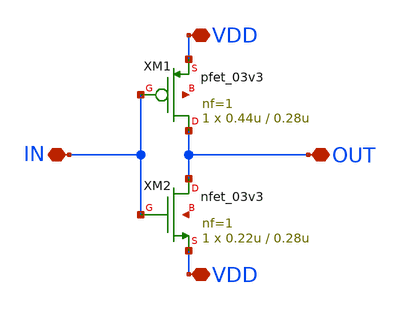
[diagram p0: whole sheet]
** sch_path: inverter.sch
**.subckt inverter OUT IN VDD VDD
*.iopin OUT
*.iopin IN
*.iopin VDD
*.iopin VDD
XM1 OUT IN VDD net1 pfet_03v3 L=0.28u W=0.44u nf=1 ad='int((nf+1)/2) * W/nf * 0.18u' as='int((nf+2)/2) * W/nf * 0.18u'
+ pd='2*int((nf+1)/2) * (W/nf + 0.18u)' ps='2*int((nf+2)/2) * (W/nf + 0.18u)' nrd='0.18u / W' nrs='0.18u / W'
+ sa=0 sb=0 sd=0 m=1
XM2 OUT IN VDD net2 nfet_03v3 L=0.28u W=0.22u nf=1 ad='int((nf+1)/2) * W/nf * 0.18u' as='int((nf+2)/2) * W/nf * 0.18u'
+ pd='2*int((nf+1)/2) * (W/nf + 0.18u)' ps='2*int((nf+2)/2) * (W/nf + 0.18u)' nrd='0.18u / W' nrs='0.18u / W'
+ sa=0 sb=0 sd=0 m=1
**.ends
.end
